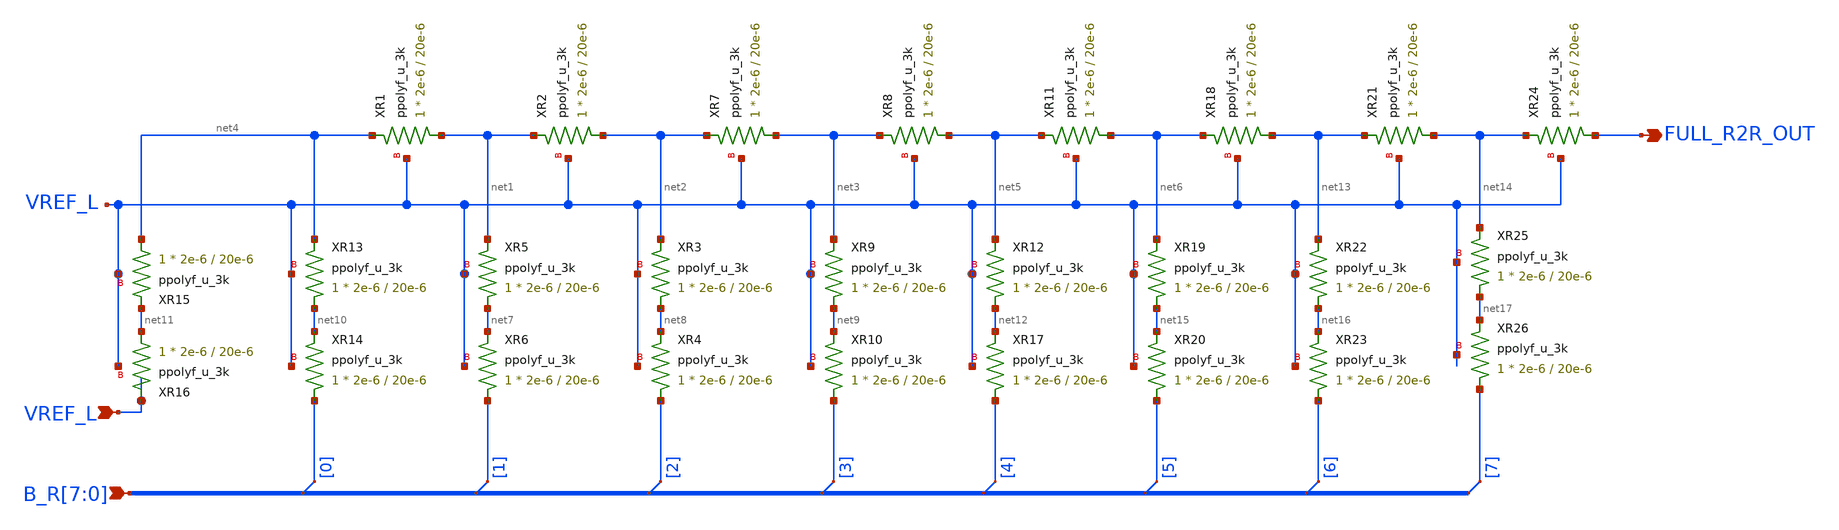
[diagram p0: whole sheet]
** sch_path: xschem/full_r2r.sch
**.subckt full_r2r FULL_R2R_OUT VREF_L B_R[7],B_R[6],B_R[5],B_R[4],B_R[3],B_R[2],B_R[1],B_R[0]
*.opin FULL_R2R_OUT
*.ipin VREF_L
*.ipin B_R[7],B_R[6],B_R[5],B_R[4],B_R[3],B_R[2],B_R[1],B_R[0]
XR1 net1 net4 VREF_L ppolyf_u_3k r_width=2e-6 r_length=20e-6 m=1
XR2 net2 net1 VREF_L ppolyf_u_3k r_width=2e-6 r_length=20e-6 m=1
XR5 net7 net1 VREF_L ppolyf_u_3k r_width=2e-6 r_length=20e-6 m=1
XR6 B_R[1] net7 VREF_L ppolyf_u_3k r_width=2e-6 r_length=20e-6 m=1
XR3 net8 net2 VREF_L ppolyf_u_3k r_width=2e-6 r_length=20e-6 m=1
XR4 B_R[2] net8 VREF_L ppolyf_u_3k r_width=2e-6 r_length=20e-6 m=1
XR7 net3 net2 VREF_L ppolyf_u_3k r_width=2e-6 r_length=20e-6 m=1
XR8 net5 net3 VREF_L ppolyf_u_3k r_width=2e-6 r_length=20e-6 m=1
XR9 net9 net3 VREF_L ppolyf_u_3k r_width=2e-6 r_length=20e-6 m=1
XR10 B_R[3] net9 VREF_L ppolyf_u_3k r_width=2e-6 r_length=20e-6 m=1
XR13 net10 net4 VREF_L ppolyf_u_3k r_width=2e-6 r_length=20e-6 m=1
XR14 B_R[0] net10 VREF_L ppolyf_u_3k r_width=2e-6 r_length=20e-6 m=1
XR15 net4 net11 VREF_L ppolyf_u_3k r_width=2e-6 r_length=20e-6 m=1
XR16 net11 VREF_L VREF_L ppolyf_u_3k r_width=2e-6 r_length=20e-6 m=1
XR11 net6 net5 VREF_L ppolyf_u_3k r_width=2e-6 r_length=20e-6 m=1
XR12 net12 net5 VREF_L ppolyf_u_3k r_width=2e-6 r_length=20e-6 m=1
XR17 B_R[4] net12 VREF_L ppolyf_u_3k r_width=2e-6 r_length=20e-6 m=1
* tap: B_R[7:0] --> B_R[0]
* tap: B_R[7:0] --> B_R[1]
* tap: B_R[7:0] --> B_R[2]
* tap: B_R[7:0] --> B_R[3]
* tap: B_R[7:0] --> B_R[4]
XR18 net13 net6 VREF_L ppolyf_u_3k r_width=2e-6 r_length=20e-6 m=1
XR19 net15 net6 VREF_L ppolyf_u_3k r_width=2e-6 r_length=20e-6 m=1
XR20 B_R[5] net15 VREF_L ppolyf_u_3k r_width=2e-6 r_length=20e-6 m=1
XR21 net14 net13 VREF_L ppolyf_u_3k r_width=2e-6 r_length=20e-6 m=1
XR22 net16 net13 VREF_L ppolyf_u_3k r_width=2e-6 r_length=20e-6 m=1
XR23 B_R[6] net16 VREF_L ppolyf_u_3k r_width=2e-6 r_length=20e-6 m=1
* tap: B_R[7:0] --> B_R[5]
* tap: B_R[7:0] --> B_R[6]
XR24 FULL_R2R_OUT net14 VREF_L ppolyf_u_3k r_width=2e-6 r_length=20e-6 m=1
* tap: B_R[7:0] --> B_R[7]
XR25 net17 net14 VREF_L ppolyf_u_3k r_width=2e-6 r_length=20e-6 m=1
XR26 B_R[7] net17 VREF_L ppolyf_u_3k r_width=2e-6 r_length=20e-6 m=1
**.ends
.end
